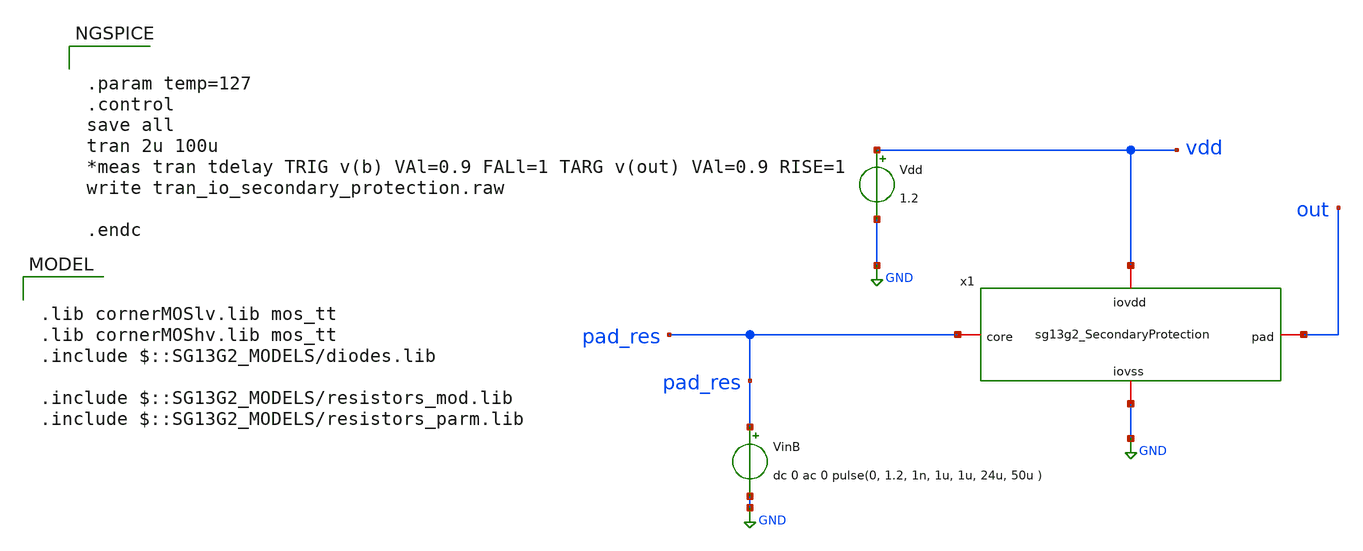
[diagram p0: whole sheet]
** sch_path: ihp-sg13g2/libs.ref/sg13g2_io/xschem/io_testbench/sg13g2_io_SecondaryProtection_tb.sch
* Copyright 2023 IHP PDK Authors
**.subckt sg13g2_io_SecondaryProtection_tb
x1 vdd out pad_res GND sg13g2_SecondaryProtection
VinB pad_res GND dc 0 ac 0 pulse(0, 1.2, 1n, 1u, 1u, 24u, 50u )
Vdd vdd GND 1.2
**** begin user architecture code

.lib cornerMOSlv.lib mos_tt
.lib cornerMOShv.lib mos_tt
.include $::SG13G2_MODELS/diodes.lib

.include $::SG13G2_MODELS/resistors_mod.lib
.include $::SG13G2_MODELS/resistors_parm.lib






.param temp=127
.control
save all
tran 2u 100u
*meas tran tdelay TRIG v(b) VAl=0.9 FALl=1 TARG v(out) VAl=0.9 RISE=1
write tran_io_secondary_protection.raw

.endc


**** end user architecture code
**.ends

* expanding   symbol:  sg13g2_SecondaryProtection.sym # of pins=4
** sym_path: ihp-sg13g2/libs.ref/sg13g2_io/xschem/sg13g2_SecondaryProtection.sym
** sch_path: ihp-sg13g2/libs.ref/sg13g2_io/xschem/sg13g2_SecondaryProtection.sch
.subckt sg13g2_SecondaryProtection iovdd pad core iovss
*.iopin iovdd
*.iopin iovss
*.iopin core
*.iopin pad
XR1 core pad sub! rppd w=1e-6 l=2e-6 m=1 b=0 mm_ok=1
XD1 iovss core dantenna l=3.1u w=0.64u
XD2 core iovdd dpantenna l=0.64u w=4.98u
.ends

.GLOBAL GND
.end
